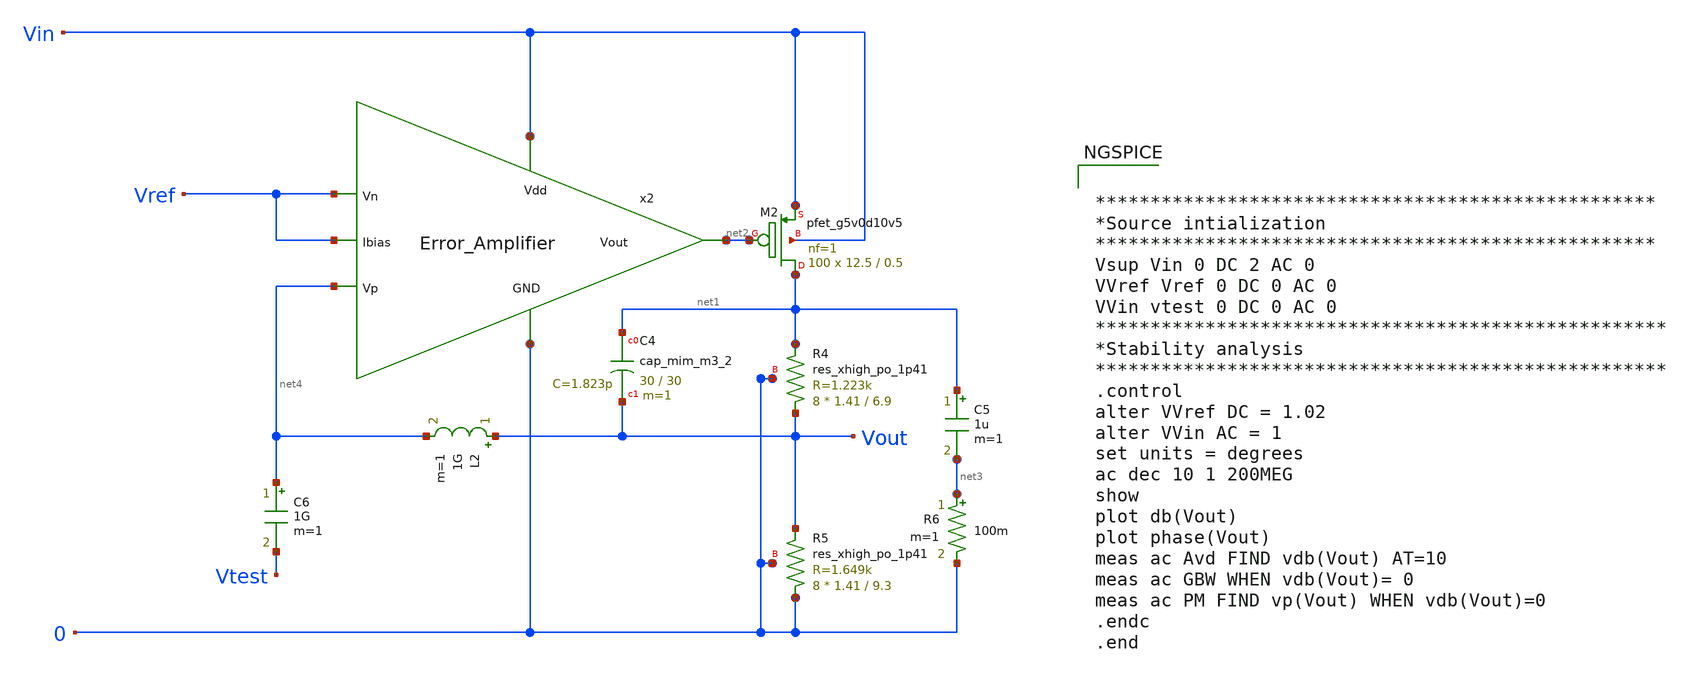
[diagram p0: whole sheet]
** sch_path: Analog_blocks/Analog_Blocks/LDO/Testbench/LDO_Miller_1.8v_meas_STB.sch
**.subckt LDO_Miller_1.8v_meas_STB
XC4 net1 Vout sky130_fd_pr__cap_mim_m3_2 W=30 L=30 MF=1 m=1
XM2 net1 net2 Vin Vin sky130_fd_pr__pfet_g5v0d10v5 L=0.5 W=12.5 nf=1 ad='int((nf+1)/2) * W/nf * 0.29'
+ as='int((nf+2)/2) * W/nf * 0.29' pd='2*int((nf+1)/2) * (W/nf + 0.29)' ps='2*int((nf+2)/2) * (W/nf + 0.29)'
+ nrd='0.29 / W' nrs='0.29 / W' sa=0 sb=0 sd=0 mult=100 m=100
XR4 Vout net1 0 sky130_fd_pr__res_xhigh_po_1p41 L=6.9 mult=8 m=8
XR5 0 Vout 0 sky130_fd_pr__res_xhigh_po_1p41 L=9.3 mult=8 m=8
C5 net1 net3 1u m=1
R6 net3 0 100m m=1
L2 Vout net4 1G m=1
C6 net4 Vtest 1G m=1
x2 Vin Vref net4 net2 Vref 0 Error_Amplifier
**** begin user architecture code


***************************************************
*Source intialization
***************************************************
Vsup Vin 0 DC 2 AC 0
VVref Vref 0 DC 0 AC 0
VVin vtest 0 DC 0 AC 0
****************************************************
*Stability analysis
****************************************************
.control
alter VVref DC = 1.02
alter VVin AC = 1
set units = degrees
ac dec 10 1 200MEG
show
plot db(Vout)
plot phase(Vout)
meas ac Avd FIND vdb(Vout) AT=10
meas ac GBW WHEN vdb(Vout)= 0
meas ac PM FIND vp(Vout) WHEN vdb(Vout)=0
.endc
.end




.param mc_mm_switch=0
.param mc_pr_switch=0
.include ~/mabrains/Analog_blocks/models/sky130A/libs.ref/sky130_fd_pr/spice/sky130_fd_pr__nfet_01v8__tt.corner.spice
.include ~/mabrains/Analog_blocks/models/sky130A/libs.ref/sky130_fd_pr/spice/sky130_fd_pr__nfet_01v8_lvt__tt.corner.spice
.include ~/mabrains/Analog_blocks/models/sky130A/libs.ref/sky130_fd_pr/spice/sky130_fd_pr__pfet_01v8__tt.corner.spice
.include ~/mabrains/Analog_blocks/models/sky130A/libs.ref/sky130_fd_pr/spice/sky130_fd_pr__nfet_03v3_nvt__tt.corner.spice
.include ~/mabrains/Analog_blocks/models/sky130A/libs.ref/sky130_fd_pr/spice/sky130_fd_pr__nfet_05v0_nvt__tt.corner.spice
.include ~/mabrains/Analog_blocks/models/sky130A/libs.ref/sky130_fd_pr/spice/sky130_fd_pr__esd_nfet_01v8__tt.corner.spice
.include ~/mabrains/Analog_blocks/models/sky130A/libs.ref/sky130_fd_pr/spice/sky130_fd_pr__pfet_01v8_lvt__tt.corner.spice
.include ~/mabrains/Analog_blocks/models/sky130A/libs.ref/sky130_fd_pr/spice/sky130_fd_pr__pfet_01v8_hvt__tt.corner.spice
.include ~/mabrains/Analog_blocks/models/sky130A/libs.ref/sky130_fd_pr/spice/sky130_fd_pr__esd_pfet_g5v0d10v5__tt.corner.spice
.include ~/mabrains/Analog_blocks/models/sky130A/libs.ref/sky130_fd_pr/spice/sky130_fd_pr__pfet_g5v0d10v5__tt.corner.spice
.include ~/mabrains/Analog_blocks/models/sky130A/libs.ref/sky130_fd_pr/spice/sky130_fd_pr__pfet_g5v0d16v0__tt.corner.spice
.include ~/mabrains/Analog_blocks/models/sky130A/libs.ref/sky130_fd_pr/spice/sky130_fd_pr__nfet_g5v0d10v5__tt.corner.spice
.include ~/mabrains/Analog_blocks/models/sky130A/libs.ref/sky130_fd_pr/spice/sky130_fd_pr__nfet_g5v0d16v0__tt_discrete.corner.spice
.include ~/mabrains/Analog_blocks/models/sky130A/libs.ref/sky130_fd_pr/spice/sky130_fd_pr__esd_nfet_g5v0d10v5__tt.corner.spice
.include ~/mabrains/Analog_blocks/models/sky130A/libs.tech/ngspice/corners/tt/nonfet.spice
* Mismatch parameters
.include ~/mabrains/Analog_blocks/models/sky130A/libs.ref/sky130_fd_pr/spice/sky130_fd_pr__nfet_01v8__mismatch.corner.spice
.include ~/mabrains/Analog_blocks/models/sky130A/libs.ref/sky130_fd_pr/spice/sky130_fd_pr__pfet_01v8__mismatch.corner.spice
.include ~/mabrains/Analog_blocks/models/sky130A/libs.ref/sky130_fd_pr/spice/sky130_fd_pr__nfet_01v8_lvt__mismatch.corner.spice
.include ~/mabrains/Analog_blocks/models/sky130A/libs.ref/sky130_fd_pr/spice/sky130_fd_pr__pfet_01v8_lvt__mismatch.corner.spice
.include ~/mabrains/Analog_blocks/models/sky130A/libs.ref/sky130_fd_pr/spice/sky130_fd_pr__pfet_01v8_hvt__mismatch.corner.spice
.include ~/mabrains/Analog_blocks/models/sky130A/libs.ref/sky130_fd_pr/spice/sky130_fd_pr__nfet_g5v0d10v5__mismatch.corner.spice
.include ~/mabrains/Analog_blocks/models/sky130A/libs.ref/sky130_fd_pr/spice/sky130_fd_pr__pfet_g5v0d10v5__mismatch.corner.spice
.include ~/mabrains/Analog_blocks/models/sky130A/libs.ref/sky130_fd_pr/spice/sky130_fd_pr__nfet_05v0_nvt__mismatch.corner.spice
.include ~/mabrains/Analog_blocks/models/sky130A/libs.ref/sky130_fd_pr/spice/sky130_fd_pr__nfet_03v3_nvt__mismatch.corner.spice
* Resistor/Capacitor
.include ~/mabrains/Analog_blocks/models/sky130A/libs.tech/ngspice/r+c/res_typical__cap_typical.spice
.include ~/mabrains/Analog_blocks/models/sky130A/libs.tech/ngspice/r+c/res_typical__cap_typical__lin.spice
* Special cells
.include ~/mabrains/Analog_blocks/models/sky130A/libs.tech/ngspice/corners/tt/specialized_cells.spice
* All models
.include ~/mabrains/Analog_blocks/models/sky130A/libs.tech/ngspice/all.spice
* Corner
.include ~/mabrains/Analog_blocks/models/sky130A/libs.tech/ngspice/corners/tt/rf.spice



**** end user architecture code
**.ends
.end
